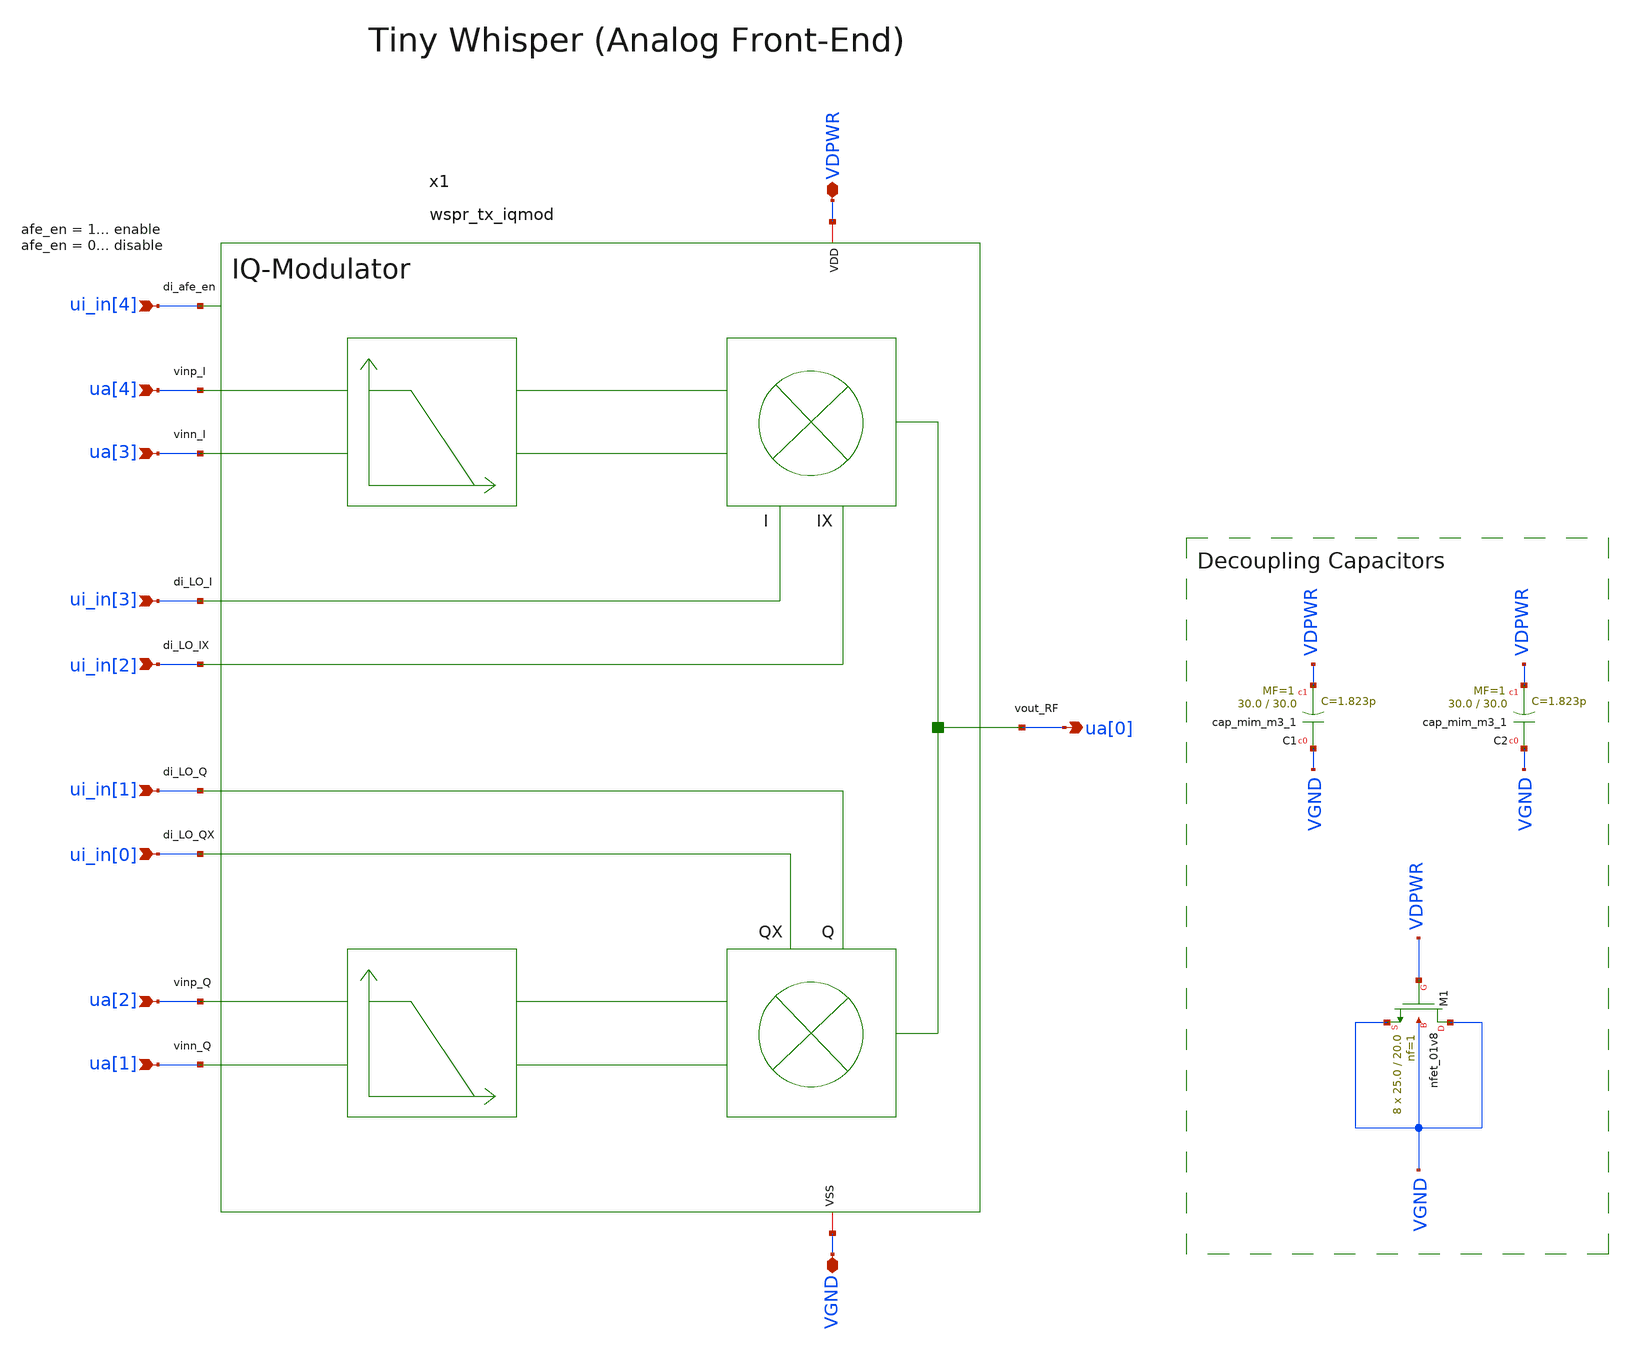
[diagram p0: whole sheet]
** sch_path: sky130/macros/iqmod/schematic/wspr_tx_iqmod_top.sch
**.subckt wspr_tx_iqmod_top VDPWR ua[0] VGND ui_in[4] ua[2] ui_in[3] ui_in[2] ui_in[1] ui_in[0]
*+ ua[1] ua[4] ua[3]
*.iopin VDPWR
*.opin ua[0]
*.iopin VGND
*.ipin ui_in[4]
*.ipin ua[2]
*.ipin ui_in[3]
*.ipin ui_in[2]
*.ipin ui_in[1]
*.ipin ui_in[0]
*.ipin ua[1]
*.ipin ua[4]
*.ipin ua[3]
XC1 VGND VDPWR sky130_fd_pr__cap_mim_m3_1 W=30.0 L=30.0 MF=1 m=1
XC2 VGND VDPWR sky130_fd_pr__cap_mim_m3_1 W=30.0 L=30.0 MF=1 m=1
XM1 VGND VDPWR VGND VGND sky130_fd_pr__nfet_01v8 L=20.0 W=25.0 nf=1 ad='int((1 + 1)/2) * 25.0 / 1 * 0.29'
+ as='int((1 + 2)/2) * 25.0 / 1 * 0.29' pd='2*int((1 + 1)/2) * (25.0 / 1 + 0.29)' ps='2*int((1 + 2)/2) * (25.0 / 1 + 0.29)'
+ nrd='0.29 / 25.0 ' nrs='0.29 / 25.0 ' sa=0 sb=0 sd=0 mult=8 m=8
x1 ui_in[4] VDPWR ua[2] ua[1] VGND ui_in[3] ui_in[2] ua[0] ua[4] ua[3] ui_in[1] ui_in[0]
+ wspr_tx_iqmod
**.ends
.end
